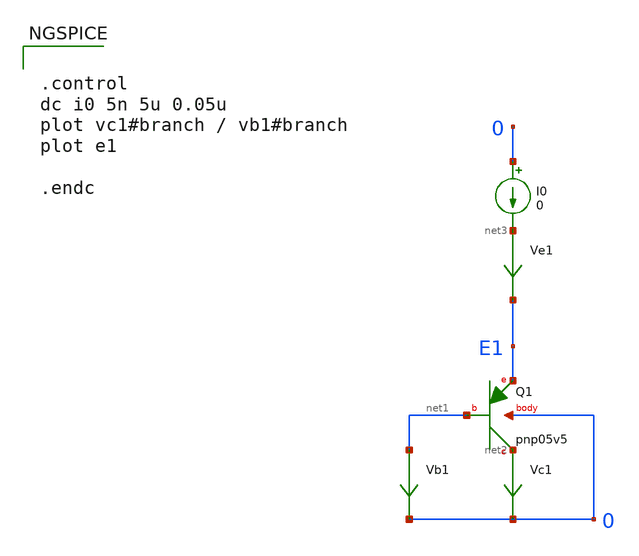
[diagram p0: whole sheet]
** sch_path: sky130_tests/test_bipolar.sch
* Copyright 2020 Stefan Frederik Schippers
* Licensed under the Apache License, Version 2.0 (the "License");
* you may not use this file except in compliance with the License.
* You may obtain a copy of the License at
* https://www.apache.org/licenses/LICENSE-2.0
* Unless required by applicable law or agreed to in writing, software
* distributed under the License is distributed on an "AS IS" BASIS,
* WITHOUT WARRANTIES OR CONDITIONS OF ANY KIND, either express or implied.
* See the License for the specific language governing permissions and
* limitations under the License.
**.subckt test_bipolar
XQ1 net2 net1 E1 0 sky130_fd_pr__pnp_05v5_W0p68L0p68
Vc1 net2 0 0
.save i(vc1)
Vb1 net1 0 0
.save i(vb1)
I0 0 net3 0
Ve1 net3 E1 0
.save i(ve1)
**** begin user architecture code


.control
dc i0 5n 5u 0.05u
plot vc1#branch / vb1#branch
plot e1

.endc


eval(
**** end user architecture code
**.ends
.end
